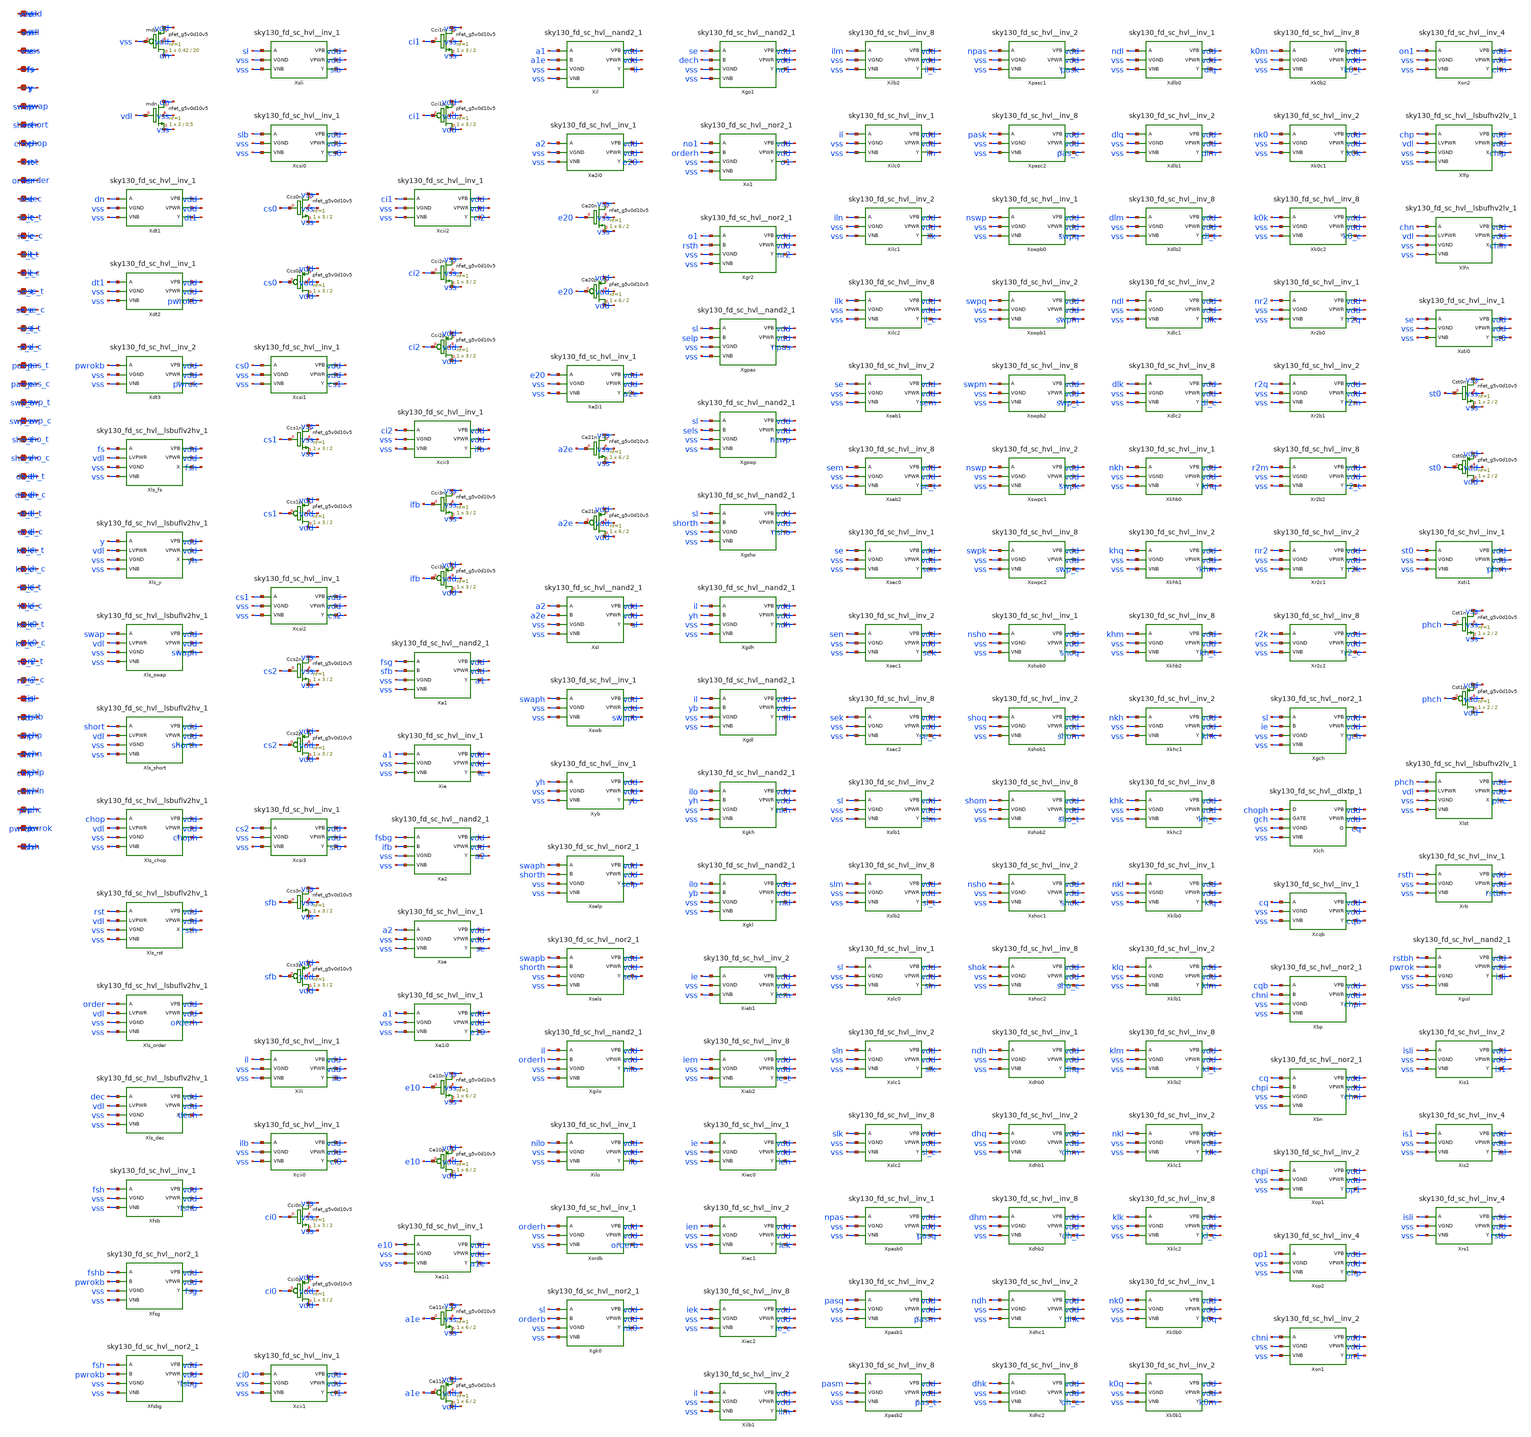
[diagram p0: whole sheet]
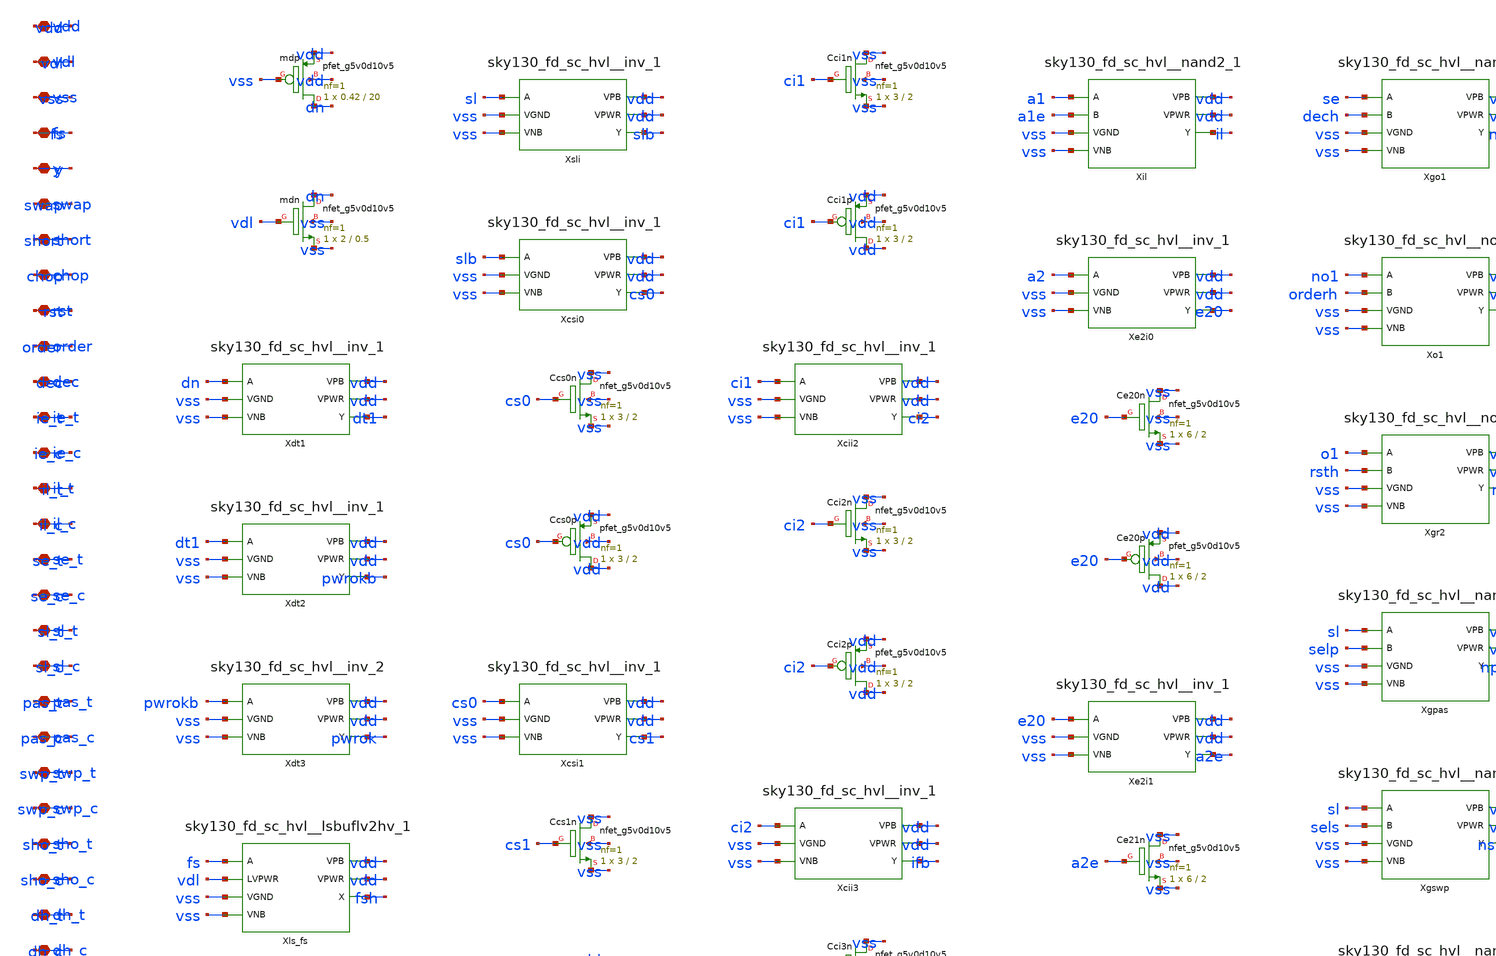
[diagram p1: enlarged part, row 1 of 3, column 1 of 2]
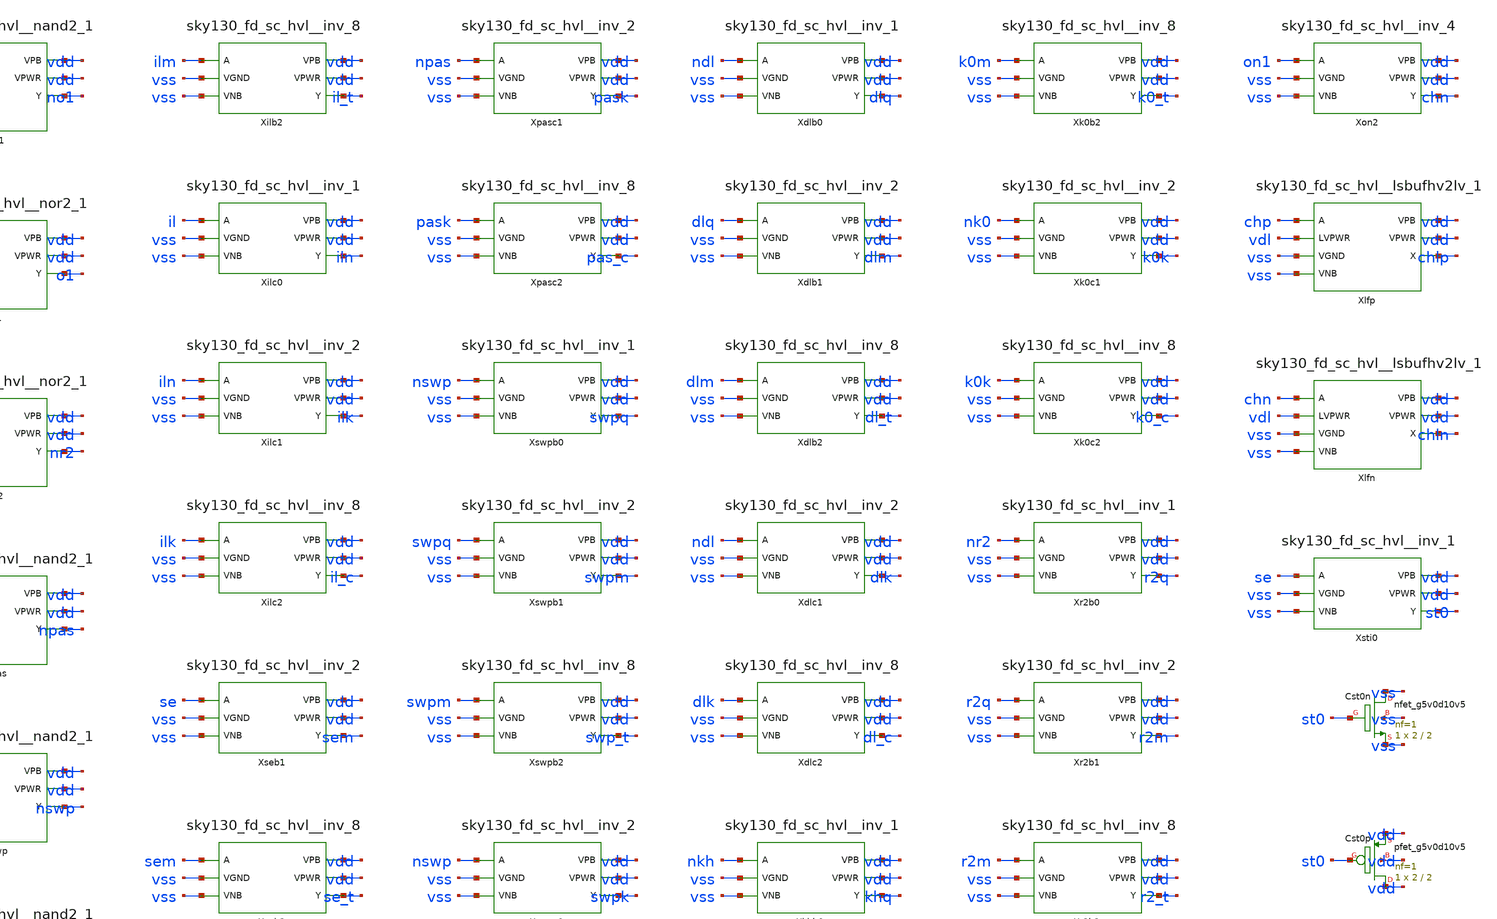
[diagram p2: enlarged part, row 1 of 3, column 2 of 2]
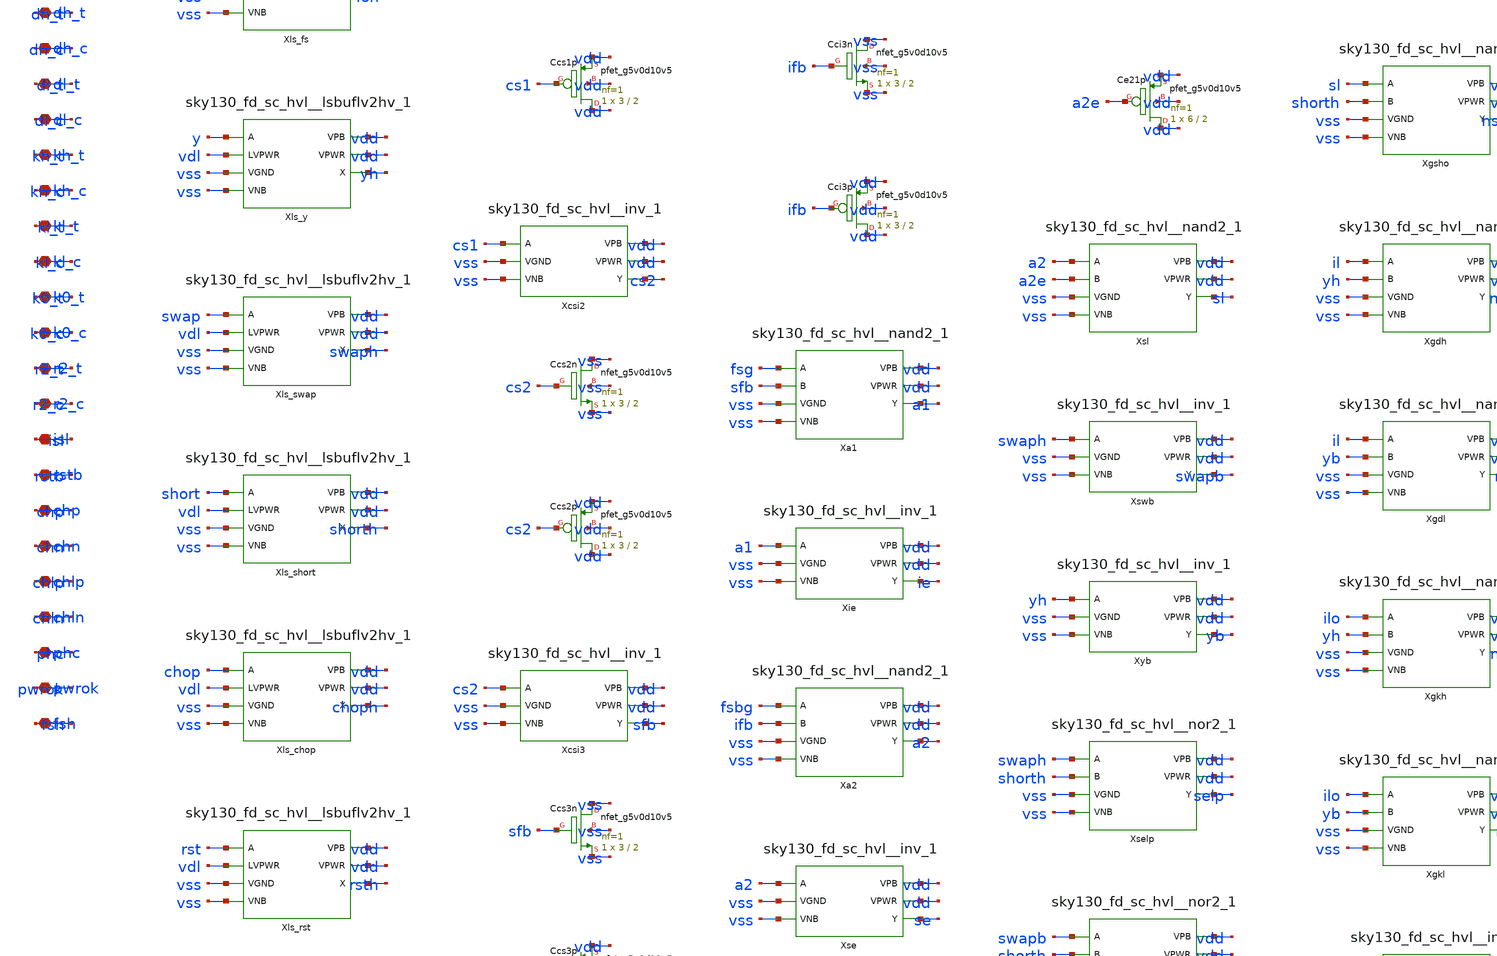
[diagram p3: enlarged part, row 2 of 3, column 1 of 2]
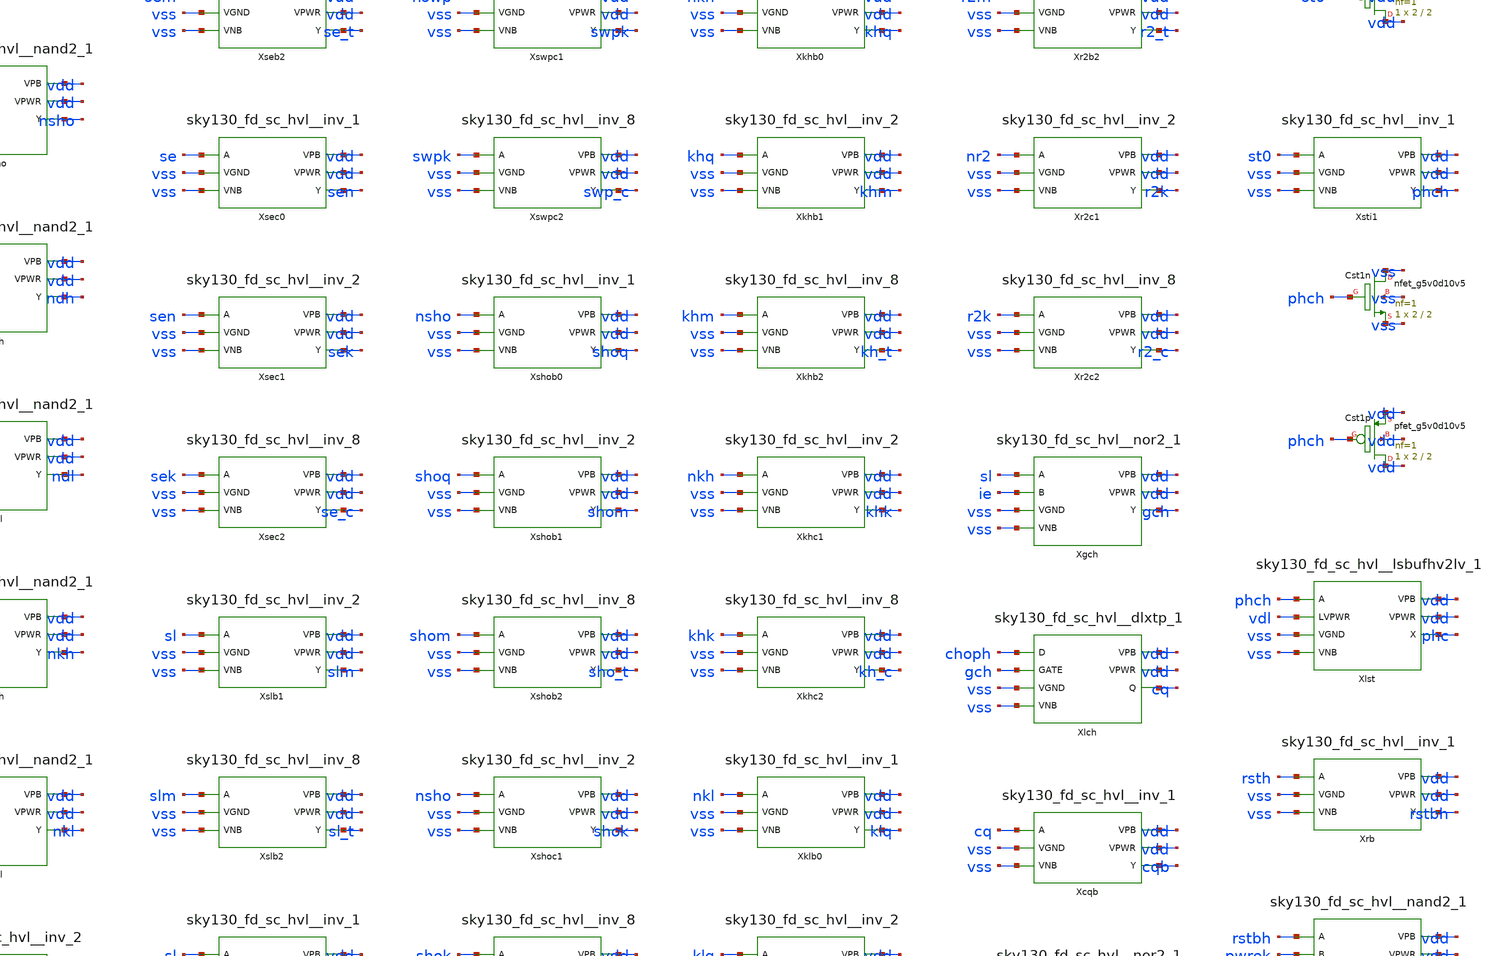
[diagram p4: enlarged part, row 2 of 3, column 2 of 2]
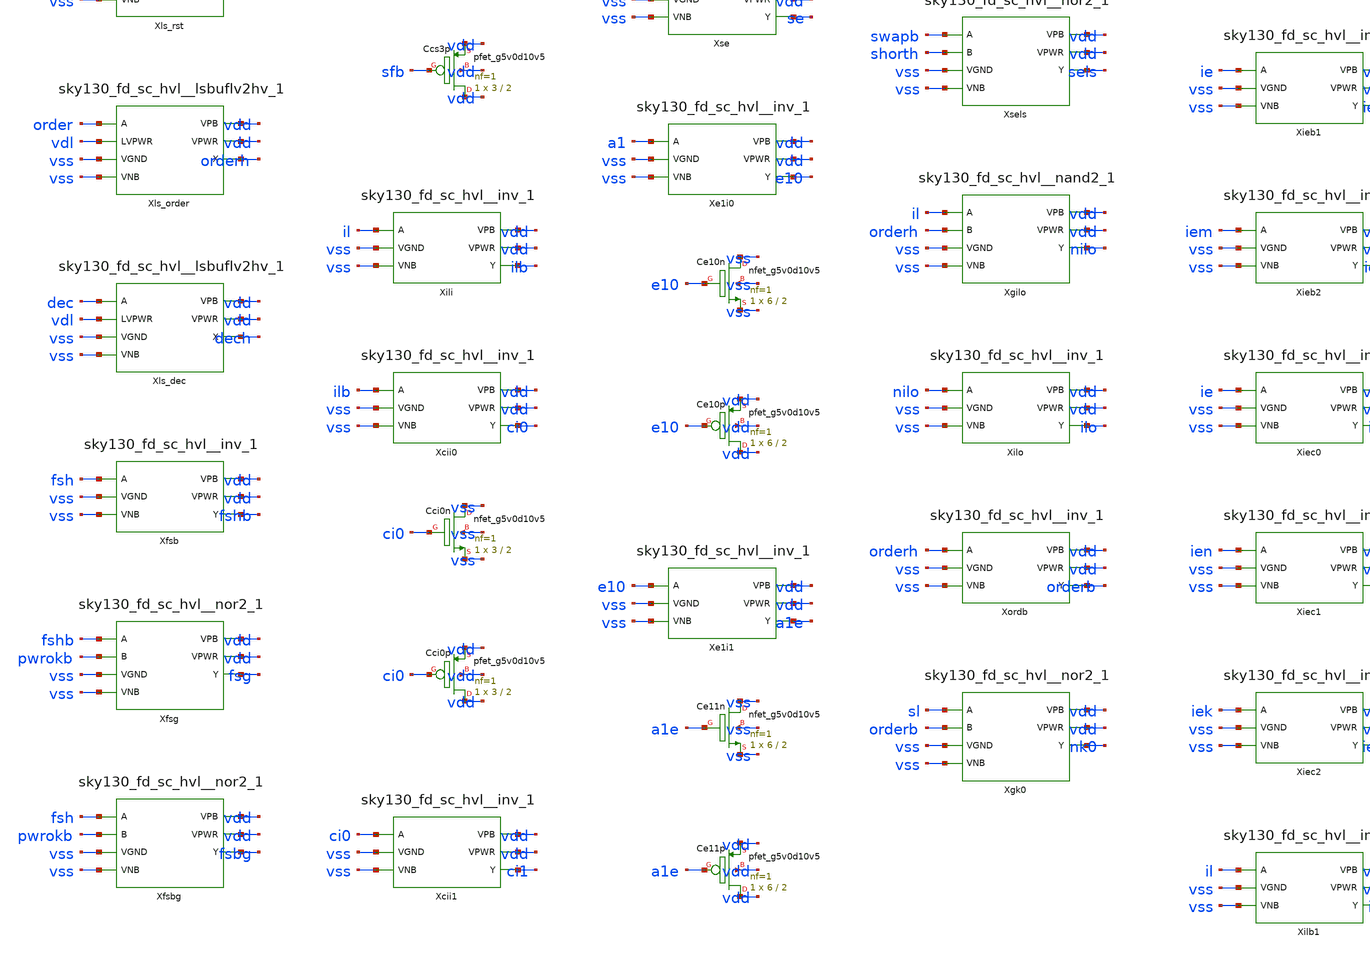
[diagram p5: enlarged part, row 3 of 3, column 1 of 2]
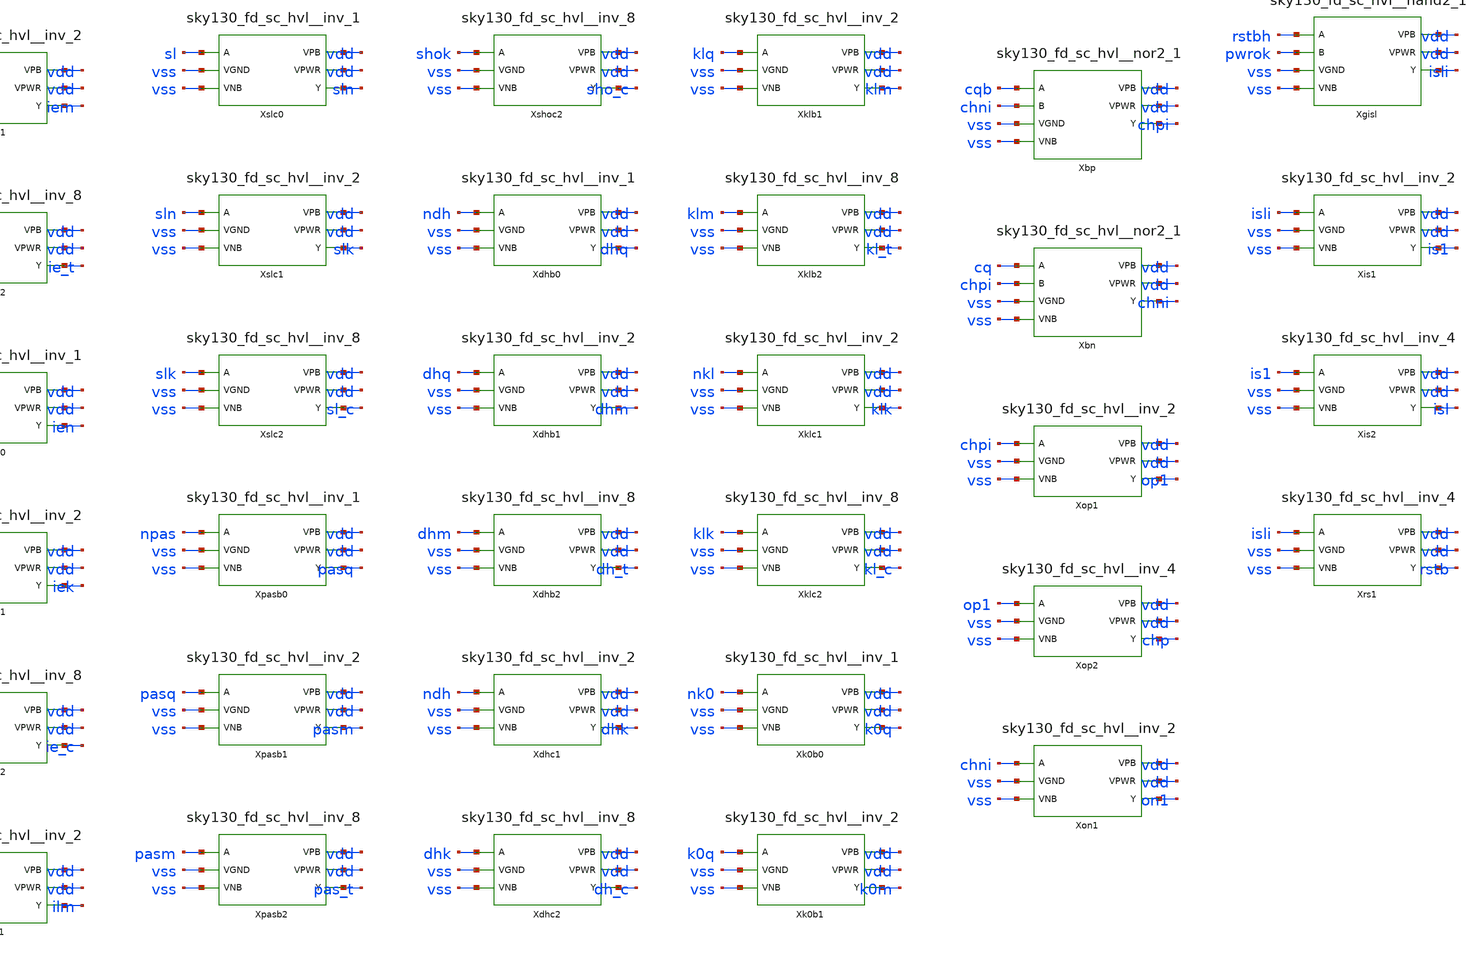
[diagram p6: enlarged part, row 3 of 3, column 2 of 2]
** sch_path: design/xschem/sch/c4_gen.sch
**.subckt c4_gen vdd vdl vss fs y swap short chop rst order dec ie_t ie_c il_t il_c se_t se_c sl_t
*+ sl_c pas_t pas_c swp_t swp_c sho_t sho_c dh_t dh_c dl_t dl_c kh_t kh_c kl_t kl_c k0_t k0_c r2_t r2_c isl
*+ rstb chp chn chlp chln phc pwrok fsh
*.iopin vdd
*.iopin vdl
*.iopin vss
*.iopin fs
*.iopin y
*.iopin swap
*.iopin short
*.iopin chop
*.iopin rst
*.iopin order
*.iopin dec
*.iopin ie_t
*.iopin ie_c
*.iopin il_t
*.iopin il_c
*.iopin se_t
*.iopin se_c
*.iopin sl_t
*.iopin sl_c
*.iopin pas_t
*.iopin pas_c
*.iopin swp_t
*.iopin swp_c
*.iopin sho_t
*.iopin sho_c
*.iopin dh_t
*.iopin dh_c
*.iopin dl_t
*.iopin dl_c
*.iopin kh_t
*.iopin kh_c
*.iopin kl_t
*.iopin kl_c
*.iopin k0_t
*.iopin k0_c
*.iopin r2_t
*.iopin r2_c
*.iopin isl
*.iopin rstb
*.iopin chp
*.iopin chn
*.iopin chlp
*.iopin chln
*.iopin phc
*.iopin pwrok
*.iopin fsh
Xmdp dn vss vdd vdd sky130_fd_pr__pfet_g5v0d10v5 L=20 W=0.42 nf=1 ad='int((1 + 1)/2) * 0.42 / 1 * 0.29'
+ as='int((1 + 2)/2) * 0.42 / 1 * 0.29' pd='2*int((1 + 1)/2) * (0.42 / 1 + 0.29)' ps='2*int((1 + 2)/2) * (0.42 / 1 + 0.29)'
+ nrd='0.29 / 0.42 ' nrs='0.29 / 0.42 ' sa=0 sb=0 sd=0 mult=1 m=1
Xmdn dn vdl vss vss sky130_fd_pr__nfet_g5v0d10v5 L=0.5 W=2 nf=1 ad='int((1 + 1)/2) * 2 / 1 * 0.29' as='int((1 + 2)/2) * 2 / 1 * 0.29'
+ pd='2*int((1 + 1)/2) * (2 / 1 + 0.29)' ps='2*int((1 + 2)/2) * (2 / 1 + 0.29)' nrd='0.29 / 2 ' nrs='0.29 / 2 '
+ sa=0 sb=0 sd=0 mult=1 m=1
Xdt1 dn vss vss vdd vdd dt1 sky130_fd_sc_hvl__inv_1
Xdt2 dt1 vss vss vdd vdd pwrokb sky130_fd_sc_hvl__inv_1
Xdt3 pwrokb vss vss vdd vdd pwrok sky130_fd_sc_hvl__inv_2
Xls_fs fs vdl vss vss vdd vdd fsh sky130_fd_sc_hvl__lsbuflv2hv_1
Xls_y y vdl vss vss vdd vdd yh sky130_fd_sc_hvl__lsbuflv2hv_1
Xls_swap swap vdl vss vss vdd vdd swaph sky130_fd_sc_hvl__lsbuflv2hv_1
Xls_short short vdl vss vss vdd vdd shorth sky130_fd_sc_hvl__lsbuflv2hv_1
Xls_chop chop vdl vss vss vdd vdd choph sky130_fd_sc_hvl__lsbuflv2hv_1
Xls_rst rst vdl vss vss vdd vdd rsth sky130_fd_sc_hvl__lsbuflv2hv_1
Xls_order order vdl vss vss vdd vdd orderh sky130_fd_sc_hvl__lsbuflv2hv_1
Xls_dec dec vdl vss vss vdd vdd dech sky130_fd_sc_hvl__lsbuflv2hv_1
Xfsb fsh vss vss vdd vdd fshb sky130_fd_sc_hvl__inv_1
Xfsg fshb pwrokb vss vss vdd vdd fsg sky130_fd_sc_hvl__nor2_1
Xfsbg fsh pwrokb vss vss vdd vdd fsbg sky130_fd_sc_hvl__nor2_1
Xsli sl vss vss vdd vdd slb sky130_fd_sc_hvl__inv_1
Xcsi0 slb vss vss vdd vdd cs0 sky130_fd_sc_hvl__inv_1
XCcs0n vss cs0 vss vss sky130_fd_pr__nfet_g5v0d10v5 L=2 W=3 nf=1 ad='int((1 + 1)/2) * 3 / 1 * 0.29' as='int((1 + 2)/2) * 3 / 1 * 0.29'
+ pd='2*int((1 + 1)/2) * (3 / 1 + 0.29)' ps='2*int((1 + 2)/2) * (3 / 1 + 0.29)' nrd='0.29 / 3 ' nrs='0.29 / 3 '
+ sa=0 sb=0 sd=0 mult=1 m=1
XCcs0p vdd cs0 vdd vdd sky130_fd_pr__pfet_g5v0d10v5 L=2 W=3 nf=1 ad='int((1 + 1)/2) * 3 / 1 * 0.29' as='int((1 + 2)/2) * 3 / 1 * 0.29'
+ pd='2*int((1 + 1)/2) * (3 / 1 + 0.29)' ps='2*int((1 + 2)/2) * (3 / 1 + 0.29)' nrd='0.29 / 3 ' nrs='0.29 / 3 '
+ sa=0 sb=0 sd=0 mult=1 m=1
Xcsi1 cs0 vss vss vdd vdd cs1 sky130_fd_sc_hvl__inv_1
XCcs1n vss cs1 vss vss sky130_fd_pr__nfet_g5v0d10v5 L=2 W=3 nf=1 ad='int((1 + 1)/2) * 3 / 1 * 0.29' as='int((1 + 2)/2) * 3 / 1 * 0.29'
+ pd='2*int((1 + 1)/2) * (3 / 1 + 0.29)' ps='2*int((1 + 2)/2) * (3 / 1 + 0.29)' nrd='0.29 / 3 ' nrs='0.29 / 3 '
+ sa=0 sb=0 sd=0 mult=1 m=1
XCcs1p vdd cs1 vdd vdd sky130_fd_pr__pfet_g5v0d10v5 L=2 W=3 nf=1 ad='int((1 + 1)/2) * 3 / 1 * 0.29' as='int((1 + 2)/2) * 3 / 1 * 0.29'
+ pd='2*int((1 + 1)/2) * (3 / 1 + 0.29)' ps='2*int((1 + 2)/2) * (3 / 1 + 0.29)' nrd='0.29 / 3 ' nrs='0.29 / 3 '
+ sa=0 sb=0 sd=0 mult=1 m=1
Xcsi2 cs1 vss vss vdd vdd cs2 sky130_fd_sc_hvl__inv_1
XCcs2n vss cs2 vss vss sky130_fd_pr__nfet_g5v0d10v5 L=2 W=3 nf=1 ad='int((1 + 1)/2) * 3 / 1 * 0.29' as='int((1 + 2)/2) * 3 / 1 * 0.29'
+ pd='2*int((1 + 1)/2) * (3 / 1 + 0.29)' ps='2*int((1 + 2)/2) * (3 / 1 + 0.29)' nrd='0.29 / 3 ' nrs='0.29 / 3 '
+ sa=0 sb=0 sd=0 mult=1 m=1
XCcs2p vdd cs2 vdd vdd sky130_fd_pr__pfet_g5v0d10v5 L=2 W=3 nf=1 ad='int((1 + 1)/2) * 3 / 1 * 0.29' as='int((1 + 2)/2) * 3 / 1 * 0.29'
+ pd='2*int((1 + 1)/2) * (3 / 1 + 0.29)' ps='2*int((1 + 2)/2) * (3 / 1 + 0.29)' nrd='0.29 / 3 ' nrs='0.29 / 3 '
+ sa=0 sb=0 sd=0 mult=1 m=1
Xcsi3 cs2 vss vss vdd vdd sfb sky130_fd_sc_hvl__inv_1
XCcs3n vss sfb vss vss sky130_fd_pr__nfet_g5v0d10v5 L=2 W=3 nf=1 ad='int((1 + 1)/2) * 3 / 1 * 0.29' as='int((1 + 2)/2) * 3 / 1 * 0.29'
+ pd='2*int((1 + 1)/2) * (3 / 1 + 0.29)' ps='2*int((1 + 2)/2) * (3 / 1 + 0.29)' nrd='0.29 / 3 ' nrs='0.29 / 3 '
+ sa=0 sb=0 sd=0 mult=1 m=1
XCcs3p vdd sfb vdd vdd sky130_fd_pr__pfet_g5v0d10v5 L=2 W=3 nf=1 ad='int((1 + 1)/2) * 3 / 1 * 0.29' as='int((1 + 2)/2) * 3 / 1 * 0.29'
+ pd='2*int((1 + 1)/2) * (3 / 1 + 0.29)' ps='2*int((1 + 2)/2) * (3 / 1 + 0.29)' nrd='0.29 / 3 ' nrs='0.29 / 3 '
+ sa=0 sb=0 sd=0 mult=1 m=1
Xili il vss vss vdd vdd ilb sky130_fd_sc_hvl__inv_1
Xcii0 ilb vss vss vdd vdd ci0 sky130_fd_sc_hvl__inv_1
XCci0n vss ci0 vss vss sky130_fd_pr__nfet_g5v0d10v5 L=2 W=3 nf=1 ad='int((1 + 1)/2) * 3 / 1 * 0.29' as='int((1 + 2)/2) * 3 / 1 * 0.29'
+ pd='2*int((1 + 1)/2) * (3 / 1 + 0.29)' ps='2*int((1 + 2)/2) * (3 / 1 + 0.29)' nrd='0.29 / 3 ' nrs='0.29 / 3 '
+ sa=0 sb=0 sd=0 mult=1 m=1
XCci0p vdd ci0 vdd vdd sky130_fd_pr__pfet_g5v0d10v5 L=2 W=3 nf=1 ad='int((1 + 1)/2) * 3 / 1 * 0.29' as='int((1 + 2)/2) * 3 / 1 * 0.29'
+ pd='2*int((1 + 1)/2) * (3 / 1 + 0.29)' ps='2*int((1 + 2)/2) * (3 / 1 + 0.29)' nrd='0.29 / 3 ' nrs='0.29 / 3 '
+ sa=0 sb=0 sd=0 mult=1 m=1
Xcii1 ci0 vss vss vdd vdd ci1 sky130_fd_sc_hvl__inv_1
XCci1n vss ci1 vss vss sky130_fd_pr__nfet_g5v0d10v5 L=2 W=3 nf=1 ad='int((1 + 1)/2) * 3 / 1 * 0.29' as='int((1 + 2)/2) * 3 / 1 * 0.29'
+ pd='2*int((1 + 1)/2) * (3 / 1 + 0.29)' ps='2*int((1 + 2)/2) * (3 / 1 + 0.29)' nrd='0.29 / 3 ' nrs='0.29 / 3 '
+ sa=0 sb=0 sd=0 mult=1 m=1
XCci1p vdd ci1 vdd vdd sky130_fd_pr__pfet_g5v0d10v5 L=2 W=3 nf=1 ad='int((1 + 1)/2) * 3 / 1 * 0.29' as='int((1 + 2)/2) * 3 / 1 * 0.29'
+ pd='2*int((1 + 1)/2) * (3 / 1 + 0.29)' ps='2*int((1 + 2)/2) * (3 / 1 + 0.29)' nrd='0.29 / 3 ' nrs='0.29 / 3 '
+ sa=0 sb=0 sd=0 mult=1 m=1
Xcii2 ci1 vss vss vdd vdd ci2 sky130_fd_sc_hvl__inv_1
XCci2n vss ci2 vss vss sky130_fd_pr__nfet_g5v0d10v5 L=2 W=3 nf=1 ad='int((1 + 1)/2) * 3 / 1 * 0.29' as='int((1 + 2)/2) * 3 / 1 * 0.29'
+ pd='2*int((1 + 1)/2) * (3 / 1 + 0.29)' ps='2*int((1 + 2)/2) * (3 / 1 + 0.29)' nrd='0.29 / 3 ' nrs='0.29 / 3 '
+ sa=0 sb=0 sd=0 mult=1 m=1
XCci2p vdd ci2 vdd vdd sky130_fd_pr__pfet_g5v0d10v5 L=2 W=3 nf=1 ad='int((1 + 1)/2) * 3 / 1 * 0.29' as='int((1 + 2)/2) * 3 / 1 * 0.29'
+ pd='2*int((1 + 1)/2) * (3 / 1 + 0.29)' ps='2*int((1 + 2)/2) * (3 / 1 + 0.29)' nrd='0.29 / 3 ' nrs='0.29 / 3 '
+ sa=0 sb=0 sd=0 mult=1 m=1
Xcii3 ci2 vss vss vdd vdd ifb sky130_fd_sc_hvl__inv_1
XCci3n vss ifb vss vss sky130_fd_pr__nfet_g5v0d10v5 L=2 W=3 nf=1 ad='int((1 + 1)/2) * 3 / 1 * 0.29' as='int((1 + 2)/2) * 3 / 1 * 0.29'
+ pd='2*int((1 + 1)/2) * (3 / 1 + 0.29)' ps='2*int((1 + 2)/2) * (3 / 1 + 0.29)' nrd='0.29 / 3 ' nrs='0.29 / 3 '
+ sa=0 sb=0 sd=0 mult=1 m=1
XCci3p vdd ifb vdd vdd sky130_fd_pr__pfet_g5v0d10v5 L=2 W=3 nf=1 ad='int((1 + 1)/2) * 3 / 1 * 0.29' as='int((1 + 2)/2) * 3 / 1 * 0.29'
+ pd='2*int((1 + 1)/2) * (3 / 1 + 0.29)' ps='2*int((1 + 2)/2) * (3 / 1 + 0.29)' nrd='0.29 / 3 ' nrs='0.29 / 3 '
+ sa=0 sb=0 sd=0 mult=1 m=1
Xa1 fsg sfb vss vss vdd vdd a1 sky130_fd_sc_hvl__nand2_1
Xie a1 vss vss vdd vdd ie sky130_fd_sc_hvl__inv_1
Xa2 fsbg ifb vss vss vdd vdd a2 sky130_fd_sc_hvl__nand2_1
Xse a2 vss vss vdd vdd se sky130_fd_sc_hvl__inv_1
Xe1i0 a1 vss vss vdd vdd e10 sky130_fd_sc_hvl__inv_1
XCe10n vss e10 vss vss sky130_fd_pr__nfet_g5v0d10v5 L=2 W=6 nf=1 ad='int((1 + 1)/2) * 6 / 1 * 0.29' as='int((1 + 2)/2) * 6 / 1 * 0.29'
+ pd='2*int((1 + 1)/2) * (6 / 1 + 0.29)' ps='2*int((1 + 2)/2) * (6 / 1 + 0.29)' nrd='0.29 / 6 ' nrs='0.29 / 6 '
+ sa=0 sb=0 sd=0 mult=1 m=1
XCe10p vdd e10 vdd vdd sky130_fd_pr__pfet_g5v0d10v5 L=2 W=6 nf=1 ad='int((1 + 1)/2) * 6 / 1 * 0.29' as='int((1 + 2)/2) * 6 / 1 * 0.29'
+ pd='2*int((1 + 1)/2) * (6 / 1 + 0.29)' ps='2*int((1 + 2)/2) * (6 / 1 + 0.29)' nrd='0.29 / 6 ' nrs='0.29 / 6 '
+ sa=0 sb=0 sd=0 mult=1 m=1
Xe1i1 e10 vss vss vdd vdd a1e sky130_fd_sc_hvl__inv_1
XCe11n vss a1e vss vss sky130_fd_pr__nfet_g5v0d10v5 L=2 W=6 nf=1 ad='int((1 + 1)/2) * 6 / 1 * 0.29' as='int((1 + 2)/2) * 6 / 1 * 0.29'
+ pd='2*int((1 + 1)/2) * (6 / 1 + 0.29)' ps='2*int((1 + 2)/2) * (6 / 1 + 0.29)' nrd='0.29 / 6 ' nrs='0.29 / 6 '
+ sa=0 sb=0 sd=0 mult=1 m=1
XCe11p vdd a1e vdd vdd sky130_fd_pr__pfet_g5v0d10v5 L=2 W=6 nf=1 ad='int((1 + 1)/2) * 6 / 1 * 0.29' as='int((1 + 2)/2) * 6 / 1 * 0.29'
+ pd='2*int((1 + 1)/2) * (6 / 1 + 0.29)' ps='2*int((1 + 2)/2) * (6 / 1 + 0.29)' nrd='0.29 / 6 ' nrs='0.29 / 6 '
+ sa=0 sb=0 sd=0 mult=1 m=1
Xil a1 a1e vss vss vdd vdd il sky130_fd_sc_hvl__nand2_1
Xe2i0 a2 vss vss vdd vdd e20 sky130_fd_sc_hvl__inv_1
XCe20n vss e20 vss vss sky130_fd_pr__nfet_g5v0d10v5 L=2 W=6 nf=1 ad='int((1 + 1)/2) * 6 / 1 * 0.29' as='int((1 + 2)/2) * 6 / 1 * 0.29'
+ pd='2*int((1 + 1)/2) * (6 / 1 + 0.29)' ps='2*int((1 + 2)/2) * (6 / 1 + 0.29)' nrd='0.29 / 6 ' nrs='0.29 / 6 '
+ sa=0 sb=0 sd=0 mult=1 m=1
XCe20p vdd e20 vdd vdd sky130_fd_pr__pfet_g5v0d10v5 L=2 W=6 nf=1 ad='int((1 + 1)/2) * 6 / 1 * 0.29' as='int((1 + 2)/2) * 6 / 1 * 0.29'
+ pd='2*int((1 + 1)/2) * (6 / 1 + 0.29)' ps='2*int((1 + 2)/2) * (6 / 1 + 0.29)' nrd='0.29 / 6 ' nrs='0.29 / 6 '
+ sa=0 sb=0 sd=0 mult=1 m=1
Xe2i1 e20 vss vss vdd vdd a2e sky130_fd_sc_hvl__inv_1
XCe21n vss a2e vss vss sky130_fd_pr__nfet_g5v0d10v5 L=2 W=6 nf=1 ad='int((1 + 1)/2) * 6 / 1 * 0.29' as='int((1 + 2)/2) * 6 / 1 * 0.29'
+ pd='2*int((1 + 1)/2) * (6 / 1 + 0.29)' ps='2*int((1 + 2)/2) * (6 / 1 + 0.29)' nrd='0.29 / 6 ' nrs='0.29 / 6 '
+ sa=0 sb=0 sd=0 mult=1 m=1
XCe21p vdd a2e vdd vdd sky130_fd_pr__pfet_g5v0d10v5 L=2 W=6 nf=1 ad='int((1 + 1)/2) * 6 / 1 * 0.29' as='int((1 + 2)/2) * 6 / 1 * 0.29'
+ pd='2*int((1 + 1)/2) * (6 / 1 + 0.29)' ps='2*int((1 + 2)/2) * (6 / 1 + 0.29)' nrd='0.29 / 6 ' nrs='0.29 / 6 '
+ sa=0 sb=0 sd=0 mult=1 m=1
Xsl a2 a2e vss vss vdd vdd sl sky130_fd_sc_hvl__nand2_1
Xswb swaph vss vss vdd vdd swapb sky130_fd_sc_hvl__inv_1
Xyb yh vss vss vdd vdd yb sky130_fd_sc_hvl__inv_1
Xselp swaph shorth vss vss vdd vdd selp sky130_fd_sc_hvl__nor2_1
Xsels swapb shorth vss vss vdd vdd sels sky130_fd_sc_hvl__nor2_1
Xgilo il orderh vss vss vdd vdd nilo sky130_fd_sc_hvl__nand2_1
Xilo nilo vss vss vdd vdd ilo sky130_fd_sc_hvl__inv_1
Xordb orderh vss vss vdd vdd orderb sky130_fd_sc_hvl__inv_1
Xgk0 sl orderb vss vss vdd vdd nk0 sky130_fd_sc_hvl__nor2_1
Xgo1 se dech vss vss vdd vdd no1 sky130_fd_sc_hvl__nand2_1
Xo1 no1 orderh vss vss vdd vdd o1 sky130_fd_sc_hvl__nor2_1
Xgr2 o1 rsth vss vss vdd vdd nr2 sky130_fd_sc_hvl__nor2_1
Xgpas sl selp vss vss vdd vdd npas sky130_fd_sc_hvl__nand2_1
Xgswp sl sels vss vss vdd vdd nswp sky130_fd_sc_hvl__nand2_1
Xgsho sl shorth vss vss vdd vdd nsho sky130_fd_sc_hvl__nand2_1
Xgdh il yh vss vss vdd vdd ndh sky130_fd_sc_hvl__nand2_1
Xgdl il yb vss vss vdd vdd ndl sky130_fd_sc_hvl__nand2_1
Xgkh ilo yh vss vss vdd vdd nkh sky130_fd_sc_hvl__nand2_1
Xgkl ilo yb vss vss vdd vdd nkl sky130_fd_sc_hvl__nand2_1
Xieb1 ie vss vss vdd vdd iem sky130_fd_sc_hvl__inv_2
Xieb2 iem vss vss vdd vdd ie_t sky130_fd_sc_hvl__inv_8
Xiec0 ie vss vss vdd vdd ien sky130_fd_sc_hvl__inv_1
Xiec1 ien vss vss vdd vdd iek sky130_fd_sc_hvl__inv_2
Xiec2 iek vss vss vdd vdd ie_c sky130_fd_sc_hvl__inv_8
Xilb1 il vss vss vdd vdd ilm sky130_fd_sc_hvl__inv_2
Xilb2 ilm vss vss vdd vdd il_t sky130_fd_sc_hvl__inv_8
Xilc0 il vss vss vdd vdd iln sky130_fd_sc_hvl__inv_1
Xilc1 iln vss vss vdd vdd ilk sky130_fd_sc_hvl__inv_2
Xilc2 ilk vss vss vdd vdd il_c sky130_fd_sc_hvl__inv_8
Xseb1 se vss vss vdd vdd sem sky130_fd_sc_hvl__inv_2
Xseb2 sem vss vss vdd vdd se_t sky130_fd_sc_hvl__inv_8
Xsec0 se vss vss vdd vdd sen sky130_fd_sc_hvl__inv_1
Xsec1 sen vss vss vdd vdd sek sky130_fd_sc_hvl__inv_2
Xsec2 sek vss vss vdd vdd se_c sky130_fd_sc_hvl__inv_8
Xslb1 sl vss vss vdd vdd slm sky130_fd_sc_hvl__inv_2
Xslb2 slm vss vss vdd vdd sl_t sky130_fd_sc_hvl__inv_8
Xslc0 sl vss vss vdd vdd sln sky130_fd_sc_hvl__inv_1
Xslc1 sln vss vss vdd vdd slk sky130_fd_sc_hvl__inv_2
Xslc2 slk vss vss vdd vdd sl_c sky130_fd_sc_hvl__inv_8
Xpasb0 npas vss vss vdd vdd pasq sky130_fd_sc_hvl__inv_1
Xpasb1 pasq vss vss vdd vdd pasm sky130_fd_sc_hvl__inv_2
Xpasb2 pasm vss vss vdd vdd pas_t sky130_fd_sc_hvl__inv_8
Xpasc1 npas vss vss vdd vdd pask sky130_fd_sc_hvl__inv_2
Xpasc2 pask vss vss vdd vdd pas_c sky130_fd_sc_hvl__inv_8
Xswpb0 nswp vss vss vdd vdd swpq sky130_fd_sc_hvl__inv_1
Xswpb1 swpq vss vss vdd vdd swpm sky130_fd_sc_hvl__inv_2
Xswpb2 swpm vss vss vdd vdd swp_t sky130_fd_sc_hvl__inv_8
Xswpc1 nswp vss vss vdd vdd swpk sky130_fd_sc_hvl__inv_2
Xswpc2 swpk vss vss vdd vdd swp_c sky130_fd_sc_hvl__inv_8
Xshob0 nsho vss vss vdd vdd shoq sky130_fd_sc_hvl__inv_1
Xshob1 shoq vss vss vdd vdd shom sky130_fd_sc_hvl__inv_2
Xshob2 shom vss vss vdd vdd sho_t sky130_fd_sc_hvl__inv_8
Xshoc1 nsho vss vss vdd vdd shok sky130_fd_sc_hvl__inv_2
Xshoc2 shok vss vss vdd vdd sho_c sky130_fd_sc_hvl__inv_8
Xdhb0 ndh vss vss vdd vdd dhq sky130_fd_sc_hvl__inv_1
Xdhb1 dhq vss vss vdd vdd dhm sky130_fd_sc_hvl__inv_2
Xdhb2 dhm vss vss vdd vdd dh_t sky130_fd_sc_hvl__inv_8
Xdhc1 ndh vss vss vdd vdd dhk sky130_fd_sc_hvl__inv_2
Xdhc2 dhk vss vss vdd vdd dh_c sky130_fd_sc_hvl__inv_8
Xdlb0 ndl vss vss vdd vdd dlq sky130_fd_sc_hvl__inv_1
Xdlb1 dlq vss vss vdd vdd dlm sky130_fd_sc_hvl__inv_2
Xdlb2 dlm vss vss vdd vdd dl_t sky130_fd_sc_hvl__inv_8
Xdlc1 ndl vss vss vdd vdd dlk sky130_fd_sc_hvl__inv_2
Xdlc2 dlk vss vss vdd vdd dl_c sky130_fd_sc_hvl__inv_8
Xkhb0 nkh vss vss vdd vdd khq sky130_fd_sc_hvl__inv_1
Xkhb1 khq vss vss vdd vdd khm sky130_fd_sc_hvl__inv_2
Xkhb2 khm vss vss vdd vdd kh_t sky130_fd_sc_hvl__inv_8
Xkhc1 nkh vss vss vdd vdd khk sky130_fd_sc_hvl__inv_2
Xkhc2 khk vss vss vdd vdd kh_c sky130_fd_sc_hvl__inv_8
Xklb0 nkl vss vss vdd vdd klq sky130_fd_sc_hvl__inv_1
Xklb1 klq vss vss vdd vdd klm sky130_fd_sc_hvl__inv_2
Xklb2 klm vss vss vdd vdd kl_t sky130_fd_sc_hvl__inv_8
Xklc1 nkl vss vss vdd vdd klk sky130_fd_sc_hvl__inv_2
Xklc2 klk vss vss vdd vdd kl_c sky130_fd_sc_hvl__inv_8
Xk0b0 nk0 vss vss vdd vdd k0q sky130_fd_sc_hvl__inv_1
Xk0b1 k0q vss vss vdd vdd k0m sky130_fd_sc_hvl__inv_2
Xk0b2 k0m vss vss vdd vdd k0_t sky130_fd_sc_hvl__inv_8
Xk0c1 nk0 vss vss vdd vdd k0k sky130_fd_sc_hvl__inv_2
Xk0c2 k0k vss vss vdd vdd k0_c sky130_fd_sc_hvl__inv_8
Xr2b0 nr2 vss vss vdd vdd r2q sky130_fd_sc_hvl__inv_1
Xr2b1 r2q vss vss vdd vdd r2m sky130_fd_sc_hvl__inv_2
Xr2b2 r2m vss vss vdd vdd r2_t sky130_fd_sc_hvl__inv_8
Xr2c1 nr2 vss vss vdd vdd r2k sky130_fd_sc_hvl__inv_2
Xr2c2 r2k vss vss vdd vdd r2_c sky130_fd_sc_hvl__inv_8
Xgch sl ie vss vss vdd vdd gch sky130_fd_sc_hvl__nor2_1
Xlch choph gch vss vss vdd vdd cq sky130_fd_sc_hvl__dlxtp_1
Xcqb cq vss vss vdd vdd cqb sky130_fd_sc_hvl__inv_1
Xbp cqb chni vss vss vdd vdd chpi sky130_fd_sc_hvl__nor2_1
Xbn cq chpi vss vss vdd vdd chni sky130_fd_sc_hvl__nor2_1
Xop1 chpi vss vss vdd vdd op1 sky130_fd_sc_hvl__inv_2
Xop2 op1 vss vss vdd vdd chp sky130_fd_sc_hvl__inv_4
Xon1 chni vss vss vdd vdd on1 sky130_fd_sc_hvl__inv_2
Xon2 on1 vss vss vdd vdd chn sky130_fd_sc_hvl__inv_4
Xlfp chp vdl vss vss vdd vdd chlp sky130_fd_sc_hvl__lsbufhv2lv_1
Xlfn chn vdl vss vss vdd vdd chln sky130_fd_sc_hvl__lsbufhv2lv_1
Xsti0 se vss vss vdd vdd st0 sky130_fd_sc_hvl__inv_1
XCst0n vss st0 vss vss sky130_fd_pr__nfet_g5v0d10v5 L=2 W=2 nf=1 ad='int((1 + 1)/2) * 2 / 1 * 0.29' as='int((1 + 2)/2) * 2 / 1 * 0.29'
+ pd='2*int((1 + 1)/2) * (2 / 1 + 0.29)' ps='2*int((1 + 2)/2) * (2 / 1 + 0.29)' nrd='0.29 / 2 ' nrs='0.29 / 2 '
+ sa=0 sb=0 sd=0 mult=1 m=1
XCst0p vdd st0 vdd vdd sky130_fd_pr__pfet_g5v0d10v5 L=2 W=2 nf=1 ad='int((1 + 1)/2) * 2 / 1 * 0.29' as='int((1 + 2)/2) * 2 / 1 * 0.29'
+ pd='2*int((1 + 1)/2) * (2 / 1 + 0.29)' ps='2*int((1 + 2)/2) * (2 / 1 + 0.29)' nrd='0.29 / 2 ' nrs='0.29 / 2 '
+ sa=0 sb=0 sd=0 mult=1 m=1
Xsti1 st0 vss vss vdd vdd phch sky130_fd_sc_hvl__inv_1
XCst1n vss phch vss vss sky130_fd_pr__nfet_g5v0d10v5 L=2 W=2 nf=1 ad='int((1 + 1)/2) * 2 / 1 * 0.29'
+ as='int((1 + 2)/2) * 2 / 1 * 0.29' pd='2*int((1 + 1)/2) * (2 / 1 + 0.29)' ps='2*int((1 + 2)/2) * (2 / 1 + 0.29)'
+ nrd='0.29 / 2 ' nrs='0.29 / 2 ' sa=0 sb=0 sd=0 mult=1 m=1
XCst1p vdd phch vdd vdd sky130_fd_pr__pfet_g5v0d10v5 L=2 W=2 nf=1 ad='int((1 + 1)/2) * 2 / 1 * 0.29'
+ as='int((1 + 2)/2) * 2 / 1 * 0.29' pd='2*int((1 + 1)/2) * (2 / 1 + 0.29)' ps='2*int((1 + 2)/2) * (2 / 1 + 0.29)'
+ nrd='0.29 / 2 ' nrs='0.29 / 2 ' sa=0 sb=0 sd=0 mult=1 m=1
Xlst phch vdl vss vss vdd vdd phc sky130_fd_sc_hvl__lsbufhv2lv_1
Xrb rsth vss vss vdd vdd rstbh sky130_fd_sc_hvl__inv_1
Xgisl rstbh pwrok vss vss vdd vdd isli sky130_fd_sc_hvl__nand2_1
Xis1 isli vss vss vdd vdd is1 sky130_fd_sc_hvl__inv_2
Xis2 is1 vss vss vdd vdd isl sky130_fd_sc_hvl__inv_4
Xrs1 isli vss vss vdd vdd rstb sky130_fd_sc_hvl__inv_4
**.ends
.end
